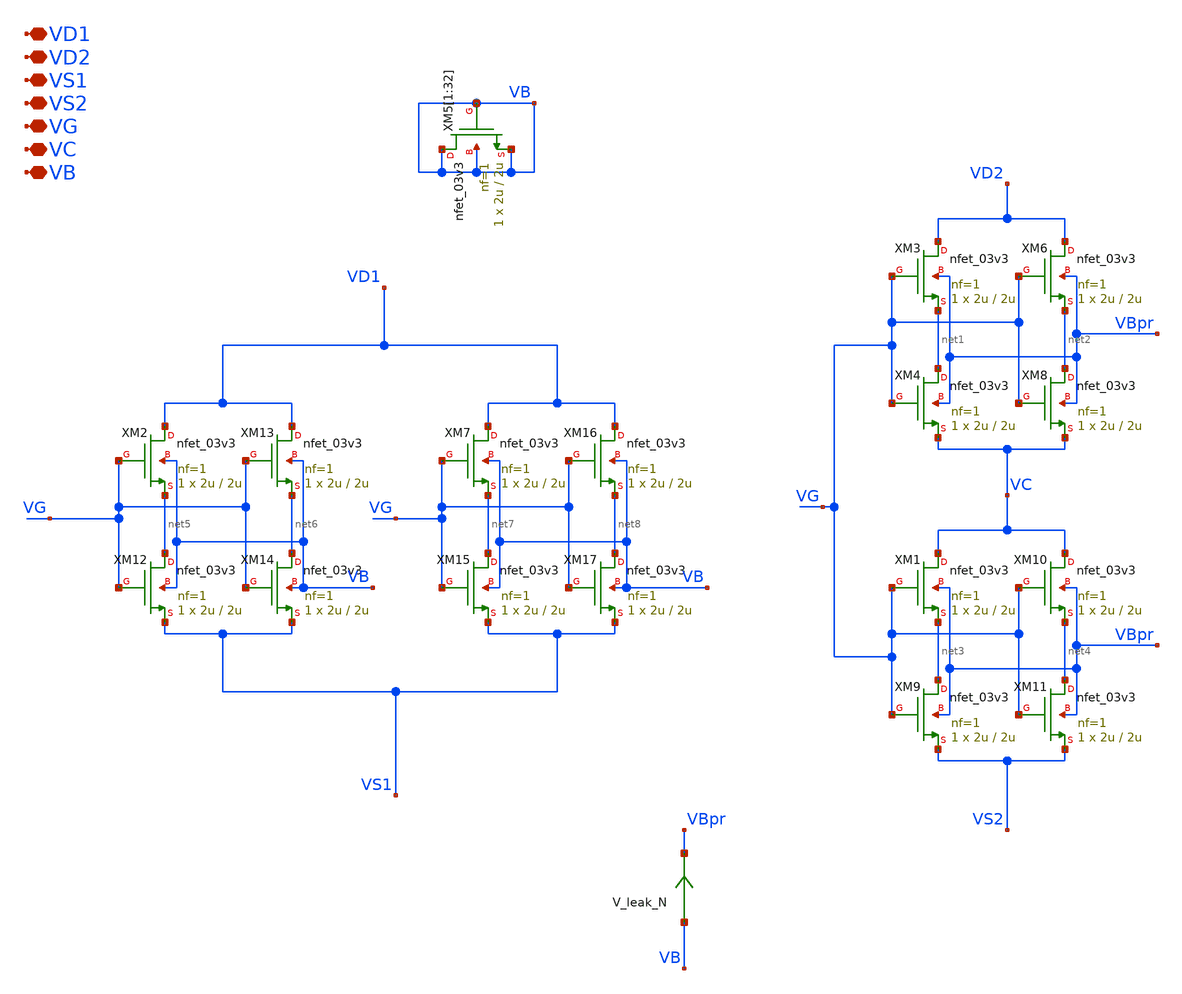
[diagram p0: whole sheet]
** sch_path: TIA_Filter/PseudoResistor/PR_nfets.sch
**.subckt PR_nfets VD1 VD2 VS1 VS2 VG VC VB
*.iopin VD1
*.iopin VD2
*.iopin VS1
*.iopin VS2
*.iopin VG
*.iopin VC
*.iopin VB
XM5[1] VB VB VB VB nfet_03v3 L=2u W=2u nf=1 ad='int((nf+1)/2) * W/nf * 0.18u' as='int((nf+2)/2) * W/nf * 0.18u'
+ pd='2*int((nf+1)/2) * (W/nf + 0.18u)' ps='2*int((nf+2)/2) * (W/nf + 0.18u)' nrd='0.18u / W' nrs='0.18u / W'
+ sa=0 sb=0 sd=0 m=1
XM5[2] VB VB VB VB nfet_03v3 L=2u W=2u nf=1 ad='int((nf+1)/2) * W/nf * 0.18u' as='int((nf+2)/2) * W/nf * 0.18u'
+ pd='2*int((nf+1)/2) * (W/nf + 0.18u)' ps='2*int((nf+2)/2) * (W/nf + 0.18u)' nrd='0.18u / W' nrs='0.18u / W'
+ sa=0 sb=0 sd=0 m=1
XM5[3] VB VB VB VB nfet_03v3 L=2u W=2u nf=1 ad='int((nf+1)/2) * W/nf * 0.18u' as='int((nf+2)/2) * W/nf * 0.18u'
+ pd='2*int((nf+1)/2) * (W/nf + 0.18u)' ps='2*int((nf+2)/2) * (W/nf + 0.18u)' nrd='0.18u / W' nrs='0.18u / W'
+ sa=0 sb=0 sd=0 m=1
XM5[4] VB VB VB VB nfet_03v3 L=2u W=2u nf=1 ad='int((nf+1)/2) * W/nf * 0.18u' as='int((nf+2)/2) * W/nf * 0.18u'
+ pd='2*int((nf+1)/2) * (W/nf + 0.18u)' ps='2*int((nf+2)/2) * (W/nf + 0.18u)' nrd='0.18u / W' nrs='0.18u / W'
+ sa=0 sb=0 sd=0 m=1
XM5[5] VB VB VB VB nfet_03v3 L=2u W=2u nf=1 ad='int((nf+1)/2) * W/nf * 0.18u' as='int((nf+2)/2) * W/nf * 0.18u'
+ pd='2*int((nf+1)/2) * (W/nf + 0.18u)' ps='2*int((nf+2)/2) * (W/nf + 0.18u)' nrd='0.18u / W' nrs='0.18u / W'
+ sa=0 sb=0 sd=0 m=1
XM5[6] VB VB VB VB nfet_03v3 L=2u W=2u nf=1 ad='int((nf+1)/2) * W/nf * 0.18u' as='int((nf+2)/2) * W/nf * 0.18u'
+ pd='2*int((nf+1)/2) * (W/nf + 0.18u)' ps='2*int((nf+2)/2) * (W/nf + 0.18u)' nrd='0.18u / W' nrs='0.18u / W'
+ sa=0 sb=0 sd=0 m=1
XM5[7] VB VB VB VB nfet_03v3 L=2u W=2u nf=1 ad='int((nf+1)/2) * W/nf * 0.18u' as='int((nf+2)/2) * W/nf * 0.18u'
+ pd='2*int((nf+1)/2) * (W/nf + 0.18u)' ps='2*int((nf+2)/2) * (W/nf + 0.18u)' nrd='0.18u / W' nrs='0.18u / W'
+ sa=0 sb=0 sd=0 m=1
XM5[8] VB VB VB VB nfet_03v3 L=2u W=2u nf=1 ad='int((nf+1)/2) * W/nf * 0.18u' as='int((nf+2)/2) * W/nf * 0.18u'
+ pd='2*int((nf+1)/2) * (W/nf + 0.18u)' ps='2*int((nf+2)/2) * (W/nf + 0.18u)' nrd='0.18u / W' nrs='0.18u / W'
+ sa=0 sb=0 sd=0 m=1
XM5[9] VB VB VB VB nfet_03v3 L=2u W=2u nf=1 ad='int((nf+1)/2) * W/nf * 0.18u' as='int((nf+2)/2) * W/nf * 0.18u'
+ pd='2*int((nf+1)/2) * (W/nf + 0.18u)' ps='2*int((nf+2)/2) * (W/nf + 0.18u)' nrd='0.18u / W' nrs='0.18u / W'
+ sa=0 sb=0 sd=0 m=1
XM5[10] VB VB VB VB nfet_03v3 L=2u W=2u nf=1 ad='int((nf+1)/2) * W/nf * 0.18u' as='int((nf+2)/2) * W/nf * 0.18u'
+ pd='2*int((nf+1)/2) * (W/nf + 0.18u)' ps='2*int((nf+2)/2) * (W/nf + 0.18u)' nrd='0.18u / W' nrs='0.18u / W'
+ sa=0 sb=0 sd=0 m=1
XM5[11] VB VB VB VB nfet_03v3 L=2u W=2u nf=1 ad='int((nf+1)/2) * W/nf * 0.18u' as='int((nf+2)/2) * W/nf * 0.18u'
+ pd='2*int((nf+1)/2) * (W/nf + 0.18u)' ps='2*int((nf+2)/2) * (W/nf + 0.18u)' nrd='0.18u / W' nrs='0.18u / W'
+ sa=0 sb=0 sd=0 m=1
XM5[12] VB VB VB VB nfet_03v3 L=2u W=2u nf=1 ad='int((nf+1)/2) * W/nf * 0.18u' as='int((nf+2)/2) * W/nf * 0.18u'
+ pd='2*int((nf+1)/2) * (W/nf + 0.18u)' ps='2*int((nf+2)/2) * (W/nf + 0.18u)' nrd='0.18u / W' nrs='0.18u / W'
+ sa=0 sb=0 sd=0 m=1
XM5[13] VB VB VB VB nfet_03v3 L=2u W=2u nf=1 ad='int((nf+1)/2) * W/nf * 0.18u' as='int((nf+2)/2) * W/nf * 0.18u'
+ pd='2*int((nf+1)/2) * (W/nf + 0.18u)' ps='2*int((nf+2)/2) * (W/nf + 0.18u)' nrd='0.18u / W' nrs='0.18u / W'
+ sa=0 sb=0 sd=0 m=1
XM5[14] VB VB VB VB nfet_03v3 L=2u W=2u nf=1 ad='int((nf+1)/2) * W/nf * 0.18u' as='int((nf+2)/2) * W/nf * 0.18u'
+ pd='2*int((nf+1)/2) * (W/nf + 0.18u)' ps='2*int((nf+2)/2) * (W/nf + 0.18u)' nrd='0.18u / W' nrs='0.18u / W'
+ sa=0 sb=0 sd=0 m=1
XM5[15] VB VB VB VB nfet_03v3 L=2u W=2u nf=1 ad='int((nf+1)/2) * W/nf * 0.18u' as='int((nf+2)/2) * W/nf * 0.18u'
+ pd='2*int((nf+1)/2) * (W/nf + 0.18u)' ps='2*int((nf+2)/2) * (W/nf + 0.18u)' nrd='0.18u / W' nrs='0.18u / W'
+ sa=0 sb=0 sd=0 m=1
XM5[16] VB VB VB VB nfet_03v3 L=2u W=2u nf=1 ad='int((nf+1)/2) * W/nf * 0.18u' as='int((nf+2)/2) * W/nf * 0.18u'
+ pd='2*int((nf+1)/2) * (W/nf + 0.18u)' ps='2*int((nf+2)/2) * (W/nf + 0.18u)' nrd='0.18u / W' nrs='0.18u / W'
+ sa=0 sb=0 sd=0 m=1
XM5[17] VB VB VB VB nfet_03v3 L=2u W=2u nf=1 ad='int((nf+1)/2) * W/nf * 0.18u' as='int((nf+2)/2) * W/nf * 0.18u'
+ pd='2*int((nf+1)/2) * (W/nf + 0.18u)' ps='2*int((nf+2)/2) * (W/nf + 0.18u)' nrd='0.18u / W' nrs='0.18u / W'
+ sa=0 sb=0 sd=0 m=1
XM5[18] VB VB VB VB nfet_03v3 L=2u W=2u nf=1 ad='int((nf+1)/2) * W/nf * 0.18u' as='int((nf+2)/2) * W/nf * 0.18u'
+ pd='2*int((nf+1)/2) * (W/nf + 0.18u)' ps='2*int((nf+2)/2) * (W/nf + 0.18u)' nrd='0.18u / W' nrs='0.18u / W'
+ sa=0 sb=0 sd=0 m=1
XM5[19] VB VB VB VB nfet_03v3 L=2u W=2u nf=1 ad='int((nf+1)/2) * W/nf * 0.18u' as='int((nf+2)/2) * W/nf * 0.18u'
+ pd='2*int((nf+1)/2) * (W/nf + 0.18u)' ps='2*int((nf+2)/2) * (W/nf + 0.18u)' nrd='0.18u / W' nrs='0.18u / W'
+ sa=0 sb=0 sd=0 m=1
XM5[20] VB VB VB VB nfet_03v3 L=2u W=2u nf=1 ad='int((nf+1)/2) * W/nf * 0.18u' as='int((nf+2)/2) * W/nf * 0.18u'
+ pd='2*int((nf+1)/2) * (W/nf + 0.18u)' ps='2*int((nf+2)/2) * (W/nf + 0.18u)' nrd='0.18u / W' nrs='0.18u / W'
+ sa=0 sb=0 sd=0 m=1
XM5[21] VB VB VB VB nfet_03v3 L=2u W=2u nf=1 ad='int((nf+1)/2) * W/nf * 0.18u' as='int((nf+2)/2) * W/nf * 0.18u'
+ pd='2*int((nf+1)/2) * (W/nf + 0.18u)' ps='2*int((nf+2)/2) * (W/nf + 0.18u)' nrd='0.18u / W' nrs='0.18u / W'
+ sa=0 sb=0 sd=0 m=1
XM5[22] VB VB VB VB nfet_03v3 L=2u W=2u nf=1 ad='int((nf+1)/2) * W/nf * 0.18u' as='int((nf+2)/2) * W/nf * 0.18u'
+ pd='2*int((nf+1)/2) * (W/nf + 0.18u)' ps='2*int((nf+2)/2) * (W/nf + 0.18u)' nrd='0.18u / W' nrs='0.18u / W'
+ sa=0 sb=0 sd=0 m=1
XM5[23] VB VB VB VB nfet_03v3 L=2u W=2u nf=1 ad='int((nf+1)/2) * W/nf * 0.18u' as='int((nf+2)/2) * W/nf * 0.18u'
+ pd='2*int((nf+1)/2) * (W/nf + 0.18u)' ps='2*int((nf+2)/2) * (W/nf + 0.18u)' nrd='0.18u / W' nrs='0.18u / W'
+ sa=0 sb=0 sd=0 m=1
XM5[24] VB VB VB VB nfet_03v3 L=2u W=2u nf=1 ad='int((nf+1)/2) * W/nf * 0.18u' as='int((nf+2)/2) * W/nf * 0.18u'
+ pd='2*int((nf+1)/2) * (W/nf + 0.18u)' ps='2*int((nf+2)/2) * (W/nf + 0.18u)' nrd='0.18u / W' nrs='0.18u / W'
+ sa=0 sb=0 sd=0 m=1
XM5[25] VB VB VB VB nfet_03v3 L=2u W=2u nf=1 ad='int((nf+1)/2) * W/nf * 0.18u' as='int((nf+2)/2) * W/nf * 0.18u'
+ pd='2*int((nf+1)/2) * (W/nf + 0.18u)' ps='2*int((nf+2)/2) * (W/nf + 0.18u)' nrd='0.18u / W' nrs='0.18u / W'
+ sa=0 sb=0 sd=0 m=1
XM5[26] VB VB VB VB nfet_03v3 L=2u W=2u nf=1 ad='int((nf+1)/2) * W/nf * 0.18u' as='int((nf+2)/2) * W/nf * 0.18u'
+ pd='2*int((nf+1)/2) * (W/nf + 0.18u)' ps='2*int((nf+2)/2) * (W/nf + 0.18u)' nrd='0.18u / W' nrs='0.18u / W'
+ sa=0 sb=0 sd=0 m=1
XM5[27] VB VB VB VB nfet_03v3 L=2u W=2u nf=1 ad='int((nf+1)/2) * W/nf * 0.18u' as='int((nf+2)/2) * W/nf * 0.18u'
+ pd='2*int((nf+1)/2) * (W/nf + 0.18u)' ps='2*int((nf+2)/2) * (W/nf + 0.18u)' nrd='0.18u / W' nrs='0.18u / W'
+ sa=0 sb=0 sd=0 m=1
XM5[28] VB VB VB VB nfet_03v3 L=2u W=2u nf=1 ad='int((nf+1)/2) * W/nf * 0.18u' as='int((nf+2)/2) * W/nf * 0.18u'
+ pd='2*int((nf+1)/2) * (W/nf + 0.18u)' ps='2*int((nf+2)/2) * (W/nf + 0.18u)' nrd='0.18u / W' nrs='0.18u / W'
+ sa=0 sb=0 sd=0 m=1
XM5[29] VB VB VB VB nfet_03v3 L=2u W=2u nf=1 ad='int((nf+1)/2) * W/nf * 0.18u' as='int((nf+2)/2) * W/nf * 0.18u'
+ pd='2*int((nf+1)/2) * (W/nf + 0.18u)' ps='2*int((nf+2)/2) * (W/nf + 0.18u)' nrd='0.18u / W' nrs='0.18u / W'
+ sa=0 sb=0 sd=0 m=1
XM5[30] VB VB VB VB nfet_03v3 L=2u W=2u nf=1 ad='int((nf+1)/2) * W/nf * 0.18u' as='int((nf+2)/2) * W/nf * 0.18u'
+ pd='2*int((nf+1)/2) * (W/nf + 0.18u)' ps='2*int((nf+2)/2) * (W/nf + 0.18u)' nrd='0.18u / W' nrs='0.18u / W'
+ sa=0 sb=0 sd=0 m=1
XM5[31] VB VB VB VB nfet_03v3 L=2u W=2u nf=1 ad='int((nf+1)/2) * W/nf * 0.18u' as='int((nf+2)/2) * W/nf * 0.18u'
+ pd='2*int((nf+1)/2) * (W/nf + 0.18u)' ps='2*int((nf+2)/2) * (W/nf + 0.18u)' nrd='0.18u / W' nrs='0.18u / W'
+ sa=0 sb=0 sd=0 m=1
XM5[32] VB VB VB VB nfet_03v3 L=2u W=2u nf=1 ad='int((nf+1)/2) * W/nf * 0.18u' as='int((nf+2)/2) * W/nf * 0.18u'
+ pd='2*int((nf+1)/2) * (W/nf + 0.18u)' ps='2*int((nf+2)/2) * (W/nf + 0.18u)' nrd='0.18u / W' nrs='0.18u / W'
+ sa=0 sb=0 sd=0 m=1
XM3 VD2 VG net1 VBpr nfet_03v3 L=2u W=2u nf=1 ad='int((nf+1)/2) * W/nf * 0.18u' as='int((nf+2)/2) * W/nf * 0.18u'
+ pd='2*int((nf+1)/2) * (W/nf + 0.18u)' ps='2*int((nf+2)/2) * (W/nf + 0.18u)' nrd='0.18u / W' nrs='0.18u / W'
+ sa=0 sb=0 sd=0 m=1
XM4 net1 VG VC VBpr nfet_03v3 L=2u W=2u nf=1 ad='int((nf+1)/2) * W/nf * 0.18u' as='int((nf+2)/2) * W/nf * 0.18u'
+ pd='2*int((nf+1)/2) * (W/nf + 0.18u)' ps='2*int((nf+2)/2) * (W/nf + 0.18u)' nrd='0.18u / W' nrs='0.18u / W'
+ sa=0 sb=0 sd=0 m=1
XM6 VD2 VG net2 VBpr nfet_03v3 L=2u W=2u nf=1 ad='int((nf+1)/2) * W/nf * 0.18u' as='int((nf+2)/2) * W/nf * 0.18u'
+ pd='2*int((nf+1)/2) * (W/nf + 0.18u)' ps='2*int((nf+2)/2) * (W/nf + 0.18u)' nrd='0.18u / W' nrs='0.18u / W'
+ sa=0 sb=0 sd=0 m=1
XM8 net2 VG VC VBpr nfet_03v3 L=2u W=2u nf=1 ad='int((nf+1)/2) * W/nf * 0.18u' as='int((nf+2)/2) * W/nf * 0.18u'
+ pd='2*int((nf+1)/2) * (W/nf + 0.18u)' ps='2*int((nf+2)/2) * (W/nf + 0.18u)' nrd='0.18u / W' nrs='0.18u / W'
+ sa=0 sb=0 sd=0 m=1
XM1 VC VG net3 VBpr nfet_03v3 L=2u W=2u nf=1 ad='int((nf+1)/2) * W/nf * 0.18u' as='int((nf+2)/2) * W/nf * 0.18u'
+ pd='2*int((nf+1)/2) * (W/nf + 0.18u)' ps='2*int((nf+2)/2) * (W/nf + 0.18u)' nrd='0.18u / W' nrs='0.18u / W'
+ sa=0 sb=0 sd=0 m=1
XM9 net3 VG VS2 VBpr nfet_03v3 L=2u W=2u nf=1 ad='int((nf+1)/2) * W/nf * 0.18u' as='int((nf+2)/2) * W/nf * 0.18u'
+ pd='2*int((nf+1)/2) * (W/nf + 0.18u)' ps='2*int((nf+2)/2) * (W/nf + 0.18u)' nrd='0.18u / W' nrs='0.18u / W'
+ sa=0 sb=0 sd=0 m=1
XM10 VC VG net4 VBpr nfet_03v3 L=2u W=2u nf=1 ad='int((nf+1)/2) * W/nf * 0.18u' as='int((nf+2)/2) * W/nf * 0.18u'
+ pd='2*int((nf+1)/2) * (W/nf + 0.18u)' ps='2*int((nf+2)/2) * (W/nf + 0.18u)' nrd='0.18u / W' nrs='0.18u / W'
+ sa=0 sb=0 sd=0 m=1
XM11 net4 VG VS2 VBpr nfet_03v3 L=2u W=2u nf=1 ad='int((nf+1)/2) * W/nf * 0.18u' as='int((nf+2)/2) * W/nf * 0.18u'
+ pd='2*int((nf+1)/2) * (W/nf + 0.18u)' ps='2*int((nf+2)/2) * (W/nf + 0.18u)' nrd='0.18u / W' nrs='0.18u / W'
+ sa=0 sb=0 sd=0 m=1
XM2 VD1 VG net5 VB nfet_03v3 L=2u W=2u nf=1 ad='int((nf+1)/2) * W/nf * 0.18u' as='int((nf+2)/2) * W/nf * 0.18u'
+ pd='2*int((nf+1)/2) * (W/nf + 0.18u)' ps='2*int((nf+2)/2) * (W/nf + 0.18u)' nrd='0.18u / W' nrs='0.18u / W'
+ sa=0 sb=0 sd=0 m=1
XM12 net5 VG VS1 VB nfet_03v3 L=2u W=2u nf=1 ad='int((nf+1)/2) * W/nf * 0.18u' as='int((nf+2)/2) * W/nf * 0.18u'
+ pd='2*int((nf+1)/2) * (W/nf + 0.18u)' ps='2*int((nf+2)/2) * (W/nf + 0.18u)' nrd='0.18u / W' nrs='0.18u / W'
+ sa=0 sb=0 sd=0 m=1
XM13 VD1 VG net6 VB nfet_03v3 L=2u W=2u nf=1 ad='int((nf+1)/2) * W/nf * 0.18u' as='int((nf+2)/2) * W/nf * 0.18u'
+ pd='2*int((nf+1)/2) * (W/nf + 0.18u)' ps='2*int((nf+2)/2) * (W/nf + 0.18u)' nrd='0.18u / W' nrs='0.18u / W'
+ sa=0 sb=0 sd=0 m=1
XM14 net6 VG VS1 VB nfet_03v3 L=2u W=2u nf=1 ad='int((nf+1)/2) * W/nf * 0.18u' as='int((nf+2)/2) * W/nf * 0.18u'
+ pd='2*int((nf+1)/2) * (W/nf + 0.18u)' ps='2*int((nf+2)/2) * (W/nf + 0.18u)' nrd='0.18u / W' nrs='0.18u / W'
+ sa=0 sb=0 sd=0 m=1
XM7 VD1 VG net7 VB nfet_03v3 L=2u W=2u nf=1 ad='int((nf+1)/2) * W/nf * 0.18u' as='int((nf+2)/2) * W/nf * 0.18u'
+ pd='2*int((nf+1)/2) * (W/nf + 0.18u)' ps='2*int((nf+2)/2) * (W/nf + 0.18u)' nrd='0.18u / W' nrs='0.18u / W'
+ sa=0 sb=0 sd=0 m=1
XM15 net7 VG VS1 VB nfet_03v3 L=2u W=2u nf=1 ad='int((nf+1)/2) * W/nf * 0.18u' as='int((nf+2)/2) * W/nf * 0.18u'
+ pd='2*int((nf+1)/2) * (W/nf + 0.18u)' ps='2*int((nf+2)/2) * (W/nf + 0.18u)' nrd='0.18u / W' nrs='0.18u / W'
+ sa=0 sb=0 sd=0 m=1
XM16 VD1 VG net8 VB nfet_03v3 L=2u W=2u nf=1 ad='int((nf+1)/2) * W/nf * 0.18u' as='int((nf+2)/2) * W/nf * 0.18u'
+ pd='2*int((nf+1)/2) * (W/nf + 0.18u)' ps='2*int((nf+2)/2) * (W/nf + 0.18u)' nrd='0.18u / W' nrs='0.18u / W'
+ sa=0 sb=0 sd=0 m=1
XM17 net8 VG VS1 VB nfet_03v3 L=2u W=2u nf=1 ad='int((nf+1)/2) * W/nf * 0.18u' as='int((nf+2)/2) * W/nf * 0.18u'
+ pd='2*int((nf+1)/2) * (W/nf + 0.18u)' ps='2*int((nf+2)/2) * (W/nf + 0.18u)' nrd='0.18u / W' nrs='0.18u / W'
+ sa=0 sb=0 sd=0 m=1
V_leak_N VB VBpr 0
.save i(v_leak_n)
**.ends
.end
